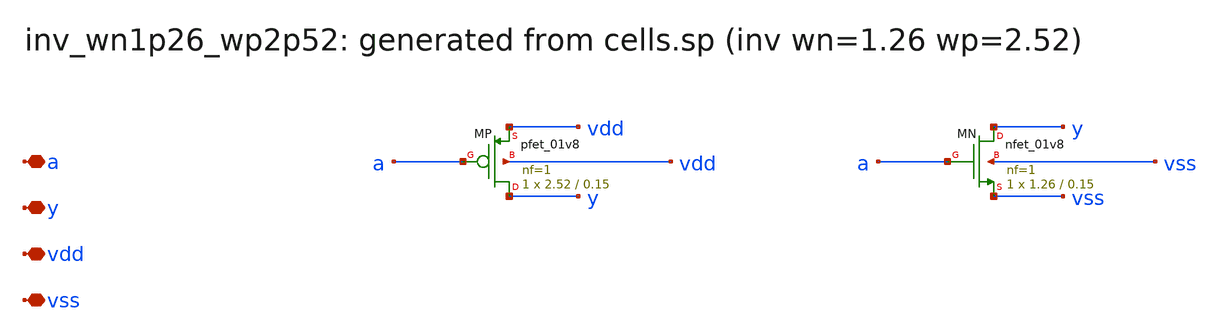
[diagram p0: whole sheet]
** sch_path: sram/xschem/inv_wn1p26_wp2p52.sch
**.subckt inv_wn1p26_wp2p52 a y vdd vss
*.iopin a
*.iopin y
*.iopin vdd
*.iopin vss
XMP y a vdd vdd sky130_fd_pr__pfet_01v8 L=0.15 W=2.52 nf=1 ad='int((nf+1)/2) * W/nf * 0.29' as='int((nf+2)/2) * W/nf * 0.29'
+ pd='2*int((nf+1)/2) * (W/nf + 0.29)' ps='2*int((nf+2)/2) * (W/nf + 0.29)' nrd='0.29 / W' nrs='0.29 / W'
+ sa=0 sb=0 sd=0 mult=1 m=1
XMN y a vss vss sky130_fd_pr__nfet_01v8 L=0.15 W=1.26 nf=1 ad='int((1 + 1)/2) * 1.26 / 1 * 0.29' as='int((1 + 2)/2) * 1.26 / 1 * 0.29'
+ pd='2*int((1 + 1)/2) * (1.26 / 1 + 0.29)' ps='2*int((1 + 2)/2) * (1.26 / 1 + 0.29)' nrd='0.29 / 1.26 '
+ nrs='0.29 / 1.26 ' sa=0 sb=0 sd=0 mult=1 m=1
**.ends
.end
